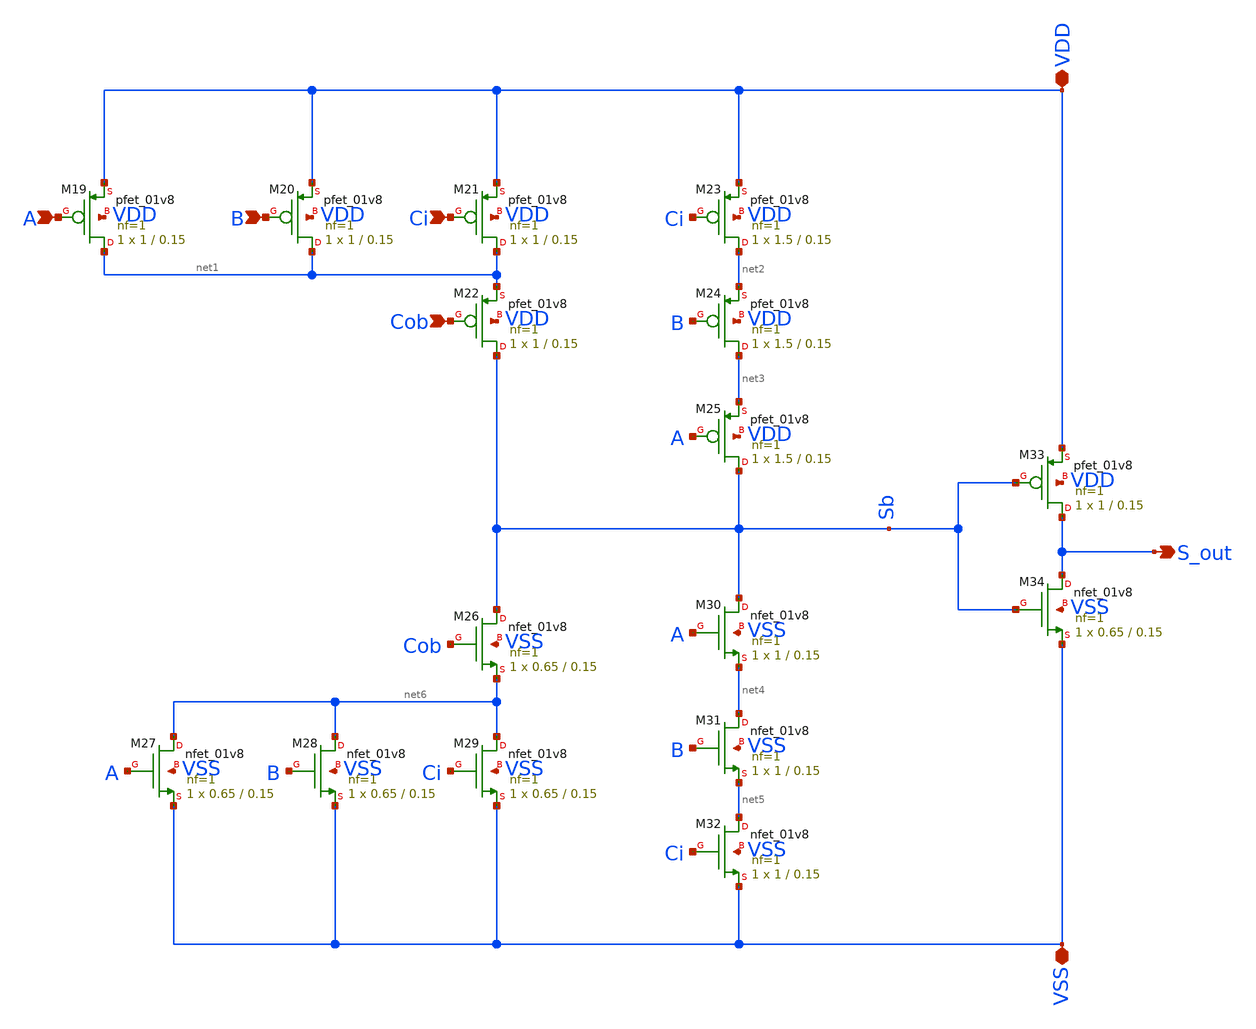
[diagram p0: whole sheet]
** sch_path: xschem/sum.sch
**.subckt sum A B Ci Cob VDD VSS S_out
*.ipin A
*.ipin B
*.ipin Ci
*.ipin Cob
*.iopin VDD
*.iopin VSS
*.opin S_out
XM19 net1 A VDD VDD sky130_fd_pr__pfet_01v8 L=0.15 W=1 nf=1 ad='int((1 + 1)/2) * 1 / 1 * 0.29' as='int((1 + 2)/2) * 1 / 1 * 0.29'
+ pd='2*int((1 + 1)/2) * (1 / 1 + 0.29)' ps='2*int((1 + 2)/2) * (1 / 1 + 0.29)' nrd='0.29 / 1 ' nrs='0.29 / 1 '
+ sa=0 sb=0 sd=0 mult=1 m=1
XM20 net1 B VDD VDD sky130_fd_pr__pfet_01v8 L=0.15 W=1 nf=1 ad='int((1 + 1)/2) * 1 / 1 * 0.29' as='int((1 + 2)/2) * 1 / 1 * 0.29'
+ pd='2*int((1 + 1)/2) * (1 / 1 + 0.29)' ps='2*int((1 + 2)/2) * (1 / 1 + 0.29)' nrd='0.29 / 1 ' nrs='0.29 / 1 '
+ sa=0 sb=0 sd=0 mult=1 m=1
XM21 net1 Ci VDD VDD sky130_fd_pr__pfet_01v8 L=0.15 W=1 nf=1 ad='int((1 + 1)/2) * 1 / 1 * 0.29' as='int((1 + 2)/2) * 1 / 1 * 0.29'
+ pd='2*int((1 + 1)/2) * (1 / 1 + 0.29)' ps='2*int((1 + 2)/2) * (1 / 1 + 0.29)' nrd='0.29 / 1 ' nrs='0.29 / 1 '
+ sa=0 sb=0 sd=0 mult=1 m=1
XM22 Sb Cob net1 VDD sky130_fd_pr__pfet_01v8 L=0.15 W=1 nf=1 ad='int((1 + 1)/2) * 1 / 1 * 0.29' as='int((1 + 2)/2) * 1 / 1 * 0.29'
+ pd='2*int((1 + 1)/2) * (1 / 1 + 0.29)' ps='2*int((1 + 2)/2) * (1 / 1 + 0.29)' nrd='0.29 / 1 ' nrs='0.29 / 1 '
+ sa=0 sb=0 sd=0 mult=1 m=1
XM23 net2 Ci VDD VDD sky130_fd_pr__pfet_01v8 L=0.15 W=1.5 nf=1 ad='int((1 + 1)/2) * 1.5 / 1 * 0.29' as='int((1 + 2)/2) * 1.5 / 1 * 0.29'
+ pd='2*int((1 + 1)/2) * (1.5 / 1 + 0.29)' ps='2*int((1 + 2)/2) * (1.5 / 1 + 0.29)' nrd='0.29 / 1.5 ' nrs='0.29 / 1.5 '
+ sa=0 sb=0 sd=0 mult=1 m=1
XM24 net3 B net2 VDD sky130_fd_pr__pfet_01v8 L=0.15 W=1.5 nf=1 ad='int((1 + 1)/2) * 1.5 / 1 * 0.29' as='int((1 + 2)/2) * 1.5 / 1 * 0.29'
+ pd='2*int((1 + 1)/2) * (1.5 / 1 + 0.29)' ps='2*int((1 + 2)/2) * (1.5 / 1 + 0.29)' nrd='0.29 / 1.5 ' nrs='0.29 / 1.5 '
+ sa=0 sb=0 sd=0 mult=1 m=1
XM25 Sb A net3 VDD sky130_fd_pr__pfet_01v8 L=0.15 W=1.5 nf=1 ad='int((1 + 1)/2) * 1.5 / 1 * 0.29' as='int((1 + 2)/2) * 1.5 / 1 * 0.29'
+ pd='2*int((1 + 1)/2) * (1.5 / 1 + 0.29)' ps='2*int((1 + 2)/2) * (1.5 / 1 + 0.29)' nrd='0.29 / 1.5 ' nrs='0.29 / 1.5 '
+ sa=0 sb=0 sd=0 mult=1 m=1
XM33 S_out Sb VDD VDD sky130_fd_pr__pfet_01v8 L=0.15 W=1 nf=1 ad='int((1 + 1)/2) * 1 / 1 * 0.29' as='int((1 + 2)/2) * 1 / 1 * 0.29'
+ pd='2*int((1 + 1)/2) * (1 / 1 + 0.29)' ps='2*int((1 + 2)/2) * (1 / 1 + 0.29)' nrd='0.29 / 1 ' nrs='0.29 / 1 '
+ sa=0 sb=0 sd=0 mult=1 m=1
XM27 net6 A VSS VSS sky130_fd_pr__nfet_01v8 L=0.15 W=0.65 nf=1 ad='int((1 + 1)/2) * 0.65 / 1 * 0.29'
+ as='int((1 + 2)/2) * 0.65 / 1 * 0.29' pd='2*int((1 + 1)/2) * (0.65 / 1 + 0.29)' ps='2*int((1 + 2)/2) * (0.65 / 1 + 0.29)'
+ nrd='0.29 / 0.65 ' nrs='0.29 / 0.65 ' sa=0 sb=0 sd=0 mult=1 m=1
XM28 net6 B VSS VSS sky130_fd_pr__nfet_01v8 L=0.15 W=0.65 nf=1 ad='int((1 + 1)/2) * 0.65 / 1 * 0.29'
+ as='int((1 + 2)/2) * 0.65 / 1 * 0.29' pd='2*int((1 + 1)/2) * (0.65 / 1 + 0.29)' ps='2*int((1 + 2)/2) * (0.65 / 1 + 0.29)'
+ nrd='0.29 / 0.65 ' nrs='0.29 / 0.65 ' sa=0 sb=0 sd=0 mult=1 m=1
XM29 net6 Ci VSS VSS sky130_fd_pr__nfet_01v8 L=0.15 W=0.65 nf=1 ad='int((1 + 1)/2) * 0.65 / 1 * 0.29'
+ as='int((1 + 2)/2) * 0.65 / 1 * 0.29' pd='2*int((1 + 1)/2) * (0.65 / 1 + 0.29)' ps='2*int((1 + 2)/2) * (0.65 / 1 + 0.29)'
+ nrd='0.29 / 0.65 ' nrs='0.29 / 0.65 ' sa=0 sb=0 sd=0 mult=1 m=1
XM26 Sb Cob net6 VSS sky130_fd_pr__nfet_01v8 L=0.15 W=0.65 nf=1 ad='int((1 + 1)/2) * 0.65 / 1 * 0.29'
+ as='int((1 + 2)/2) * 0.65 / 1 * 0.29' pd='2*int((1 + 1)/2) * (0.65 / 1 + 0.29)' ps='2*int((1 + 2)/2) * (0.65 / 1 + 0.29)'
+ nrd='0.29 / 0.65 ' nrs='0.29 / 0.65 ' sa=0 sb=0 sd=0 mult=1 m=1
XM31 net4 B net5 VSS sky130_fd_pr__nfet_01v8 L=0.15 W=1 nf=1 ad='int((1 + 1)/2) * 1 / 1 * 0.29' as='int((1 + 2)/2) * 1 / 1 * 0.29'
+ pd='2*int((1 + 1)/2) * (1 / 1 + 0.29)' ps='2*int((1 + 2)/2) * (1 / 1 + 0.29)' nrd='0.29 / 1 ' nrs='0.29 / 1 '
+ sa=0 sb=0 sd=0 mult=1 m=1
XM30 Sb A net4 VSS sky130_fd_pr__nfet_01v8 L=0.15 W=1 nf=1 ad='int((1 + 1)/2) * 1 / 1 * 0.29' as='int((1 + 2)/2) * 1 / 1 * 0.29'
+ pd='2*int((1 + 1)/2) * (1 / 1 + 0.29)' ps='2*int((1 + 2)/2) * (1 / 1 + 0.29)' nrd='0.29 / 1 ' nrs='0.29 / 1 '
+ sa=0 sb=0 sd=0 mult=1 m=1
XM32 net5 Ci VSS VSS sky130_fd_pr__nfet_01v8 L=0.15 W=1 nf=1 ad='int((1 + 1)/2) * 1 / 1 * 0.29' as='int((1 + 2)/2) * 1 / 1 * 0.29'
+ pd='2*int((1 + 1)/2) * (1 / 1 + 0.29)' ps='2*int((1 + 2)/2) * (1 / 1 + 0.29)' nrd='0.29 / 1 ' nrs='0.29 / 1 '
+ sa=0 sb=0 sd=0 mult=1 m=1
XM34 S_out Sb VSS VSS sky130_fd_pr__nfet_01v8 L=0.15 W=0.65 nf=1 ad='int((1 + 1)/2) * 0.65 / 1 * 0.29'
+ as='int((1 + 2)/2) * 0.65 / 1 * 0.29' pd='2*int((1 + 1)/2) * (0.65 / 1 + 0.29)' ps='2*int((1 + 2)/2) * (0.65 / 1 + 0.29)'
+ nrd='0.29 / 0.65 ' nrs='0.29 / 0.65 ' sa=0 sb=0 sd=0 mult=1 m=1
**.ends
.end
